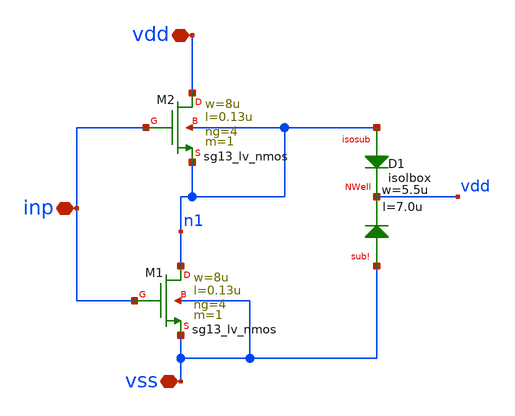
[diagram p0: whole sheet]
** sch_path: deepNWell/schematic/nmos_iso.sch
**.subckt nmos_iso inp vdd vss
*.iopin inp
*.iopin vdd
*.iopin vss
XM2 vdd inp n1 n1 sg13_lv_nmos w=8u l=0.13u ng=4 m=1 mm_ok=1
XM1 n1 inp vss vss sg13_lv_nmos w=8u l=0.13u ng=4 m=1 mm_ok=1
XD1 n1 vdd vss isolbox l=7.0u w=5.5u
**.ends
.end
